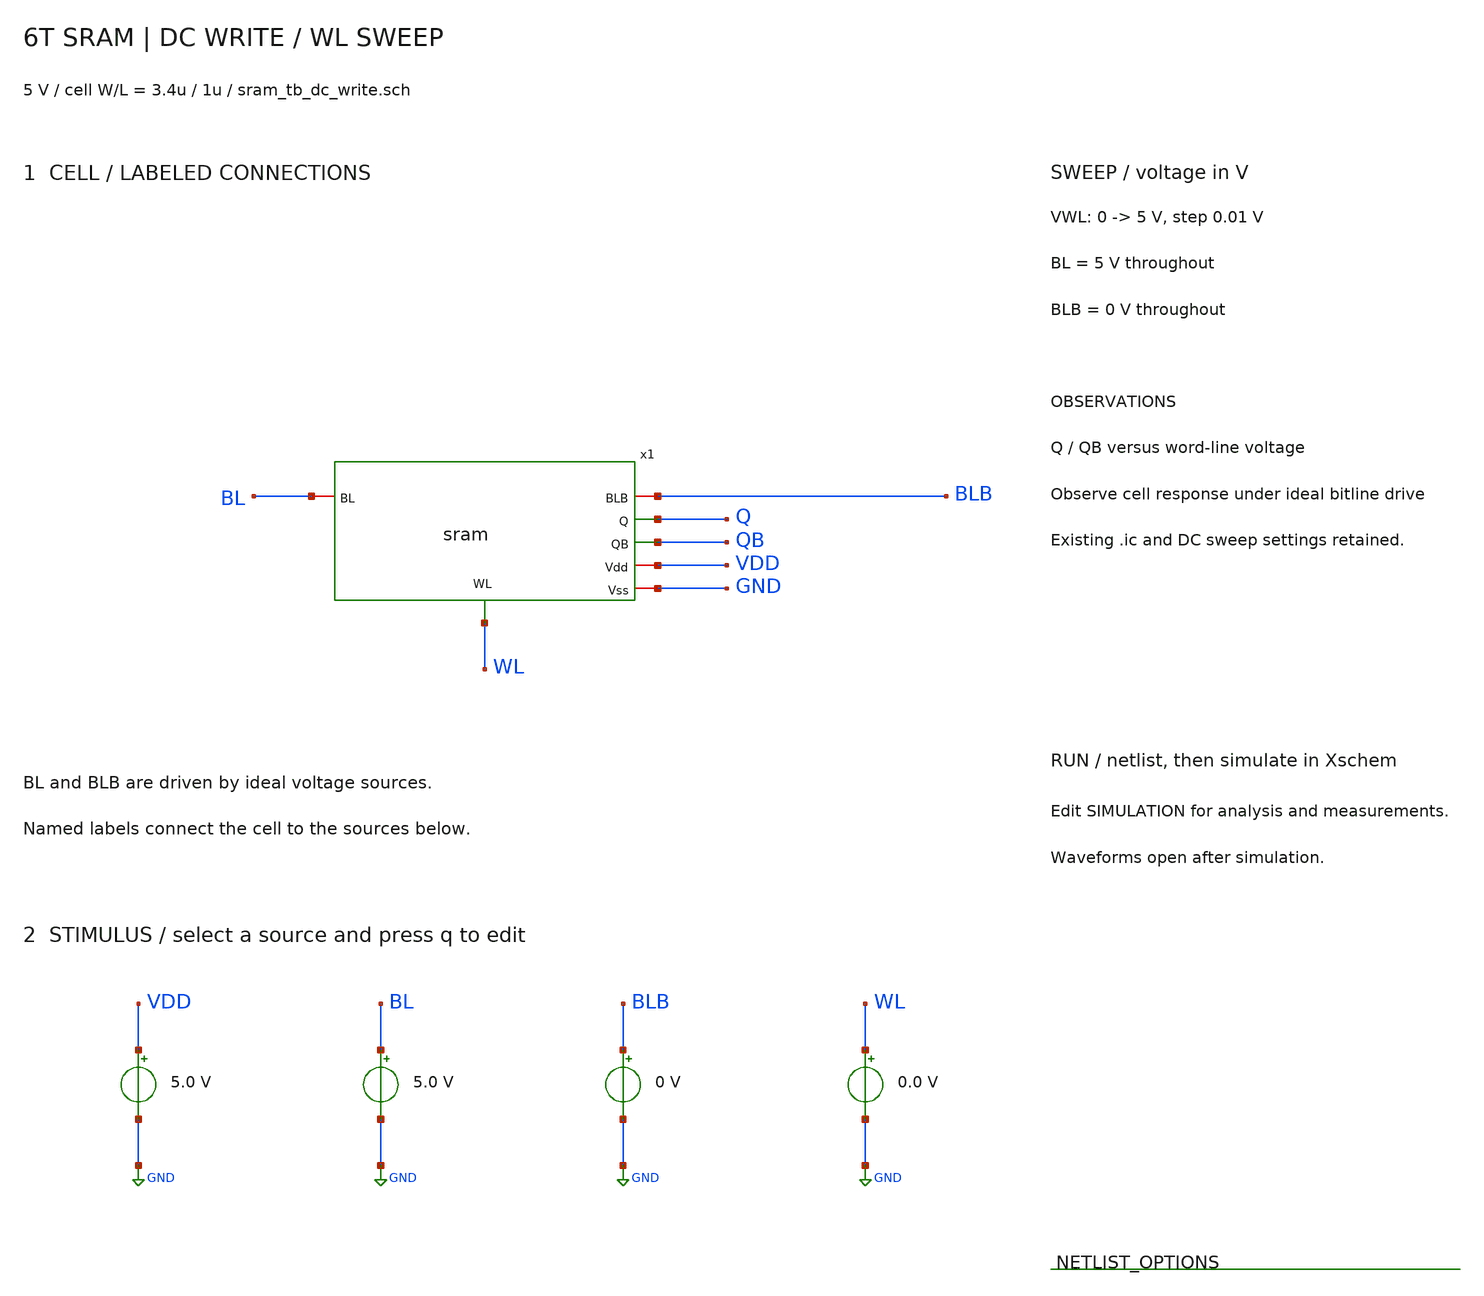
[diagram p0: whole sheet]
** sch_path: member_project/SRAM/PenguinEino/learning/schematics/sram_tb_dc_write.sch
**.subckt sram_tb_dc_write
x1 WL VDD BLB Q QB BL GND sram
Vdd VDD GND 5.0
VBL BL GND 5.0
VBLB BLB GND 0
VWL WL GND 0.0
**** begin user architecture code
 .include $::LIB/ip62_models

.ic v(Q) = 0 v(QB)=5

.control
save all

dc VWL 0 5 0.01

plot v(Q) v(QB) v(WL)

.endc

**** end user architecture code
**.ends
.GLOBAL GND
.end
